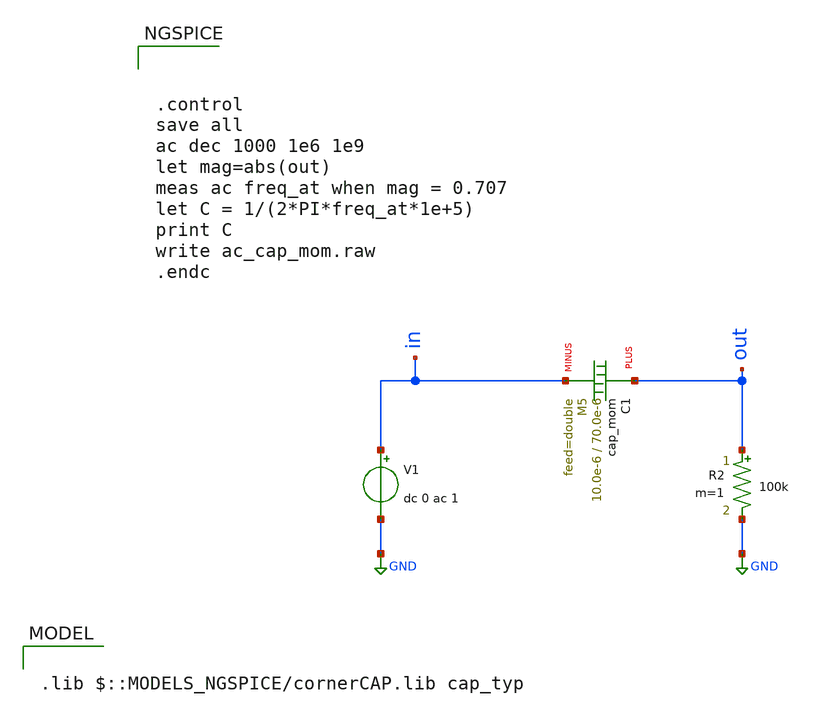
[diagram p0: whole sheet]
** sch_path: ihp-sg13g2/libs.tech/xschem/sg13g2_tests/ac_cap_mom.sch
* Copyright 2021 Stefan Frederik Schippers
* Licensed under the Apache License, Version 2.0 (the "License");
* you may not use this file except in compliance with the License.
* You may obtain a copy of the License at
* https://www.apache.org/licenses/LICENSE-2.0
* Unless required by applicable law or agreed to in writing, software
* distributed under the License is distributed on an "AS IS" BASIS,
* WITHOUT WARRANTIES OR CONDITIONS OF ANY KIND, either express or implied.
* See the License for the specific language governing permissions and
* limitations under the License.
* Copyright 2026 IHP PDK Authors
**.subckt ac_cap_mom
V1 in GND dc 0 ac 1
R2 out GND 100k m=1
XC1 out in cap_mom w=10.0e-6 l=70.0e-6 mmin=1 mmax=5 feed=double
**** begin user architecture code



.control
save all
ac dec 1000 1e6 1e9
let mag=abs(out)
meas ac freq_at when mag = 0.707
let C = 1/(2*PI*freq_at*1e+5)
print C
write ac_cap_mom.raw
.endc



.lib $::MODELS_NGSPICE/cornerCAP.lib cap_typ

**** end user architecture code
**.ends
.GLOBAL GND
.end
